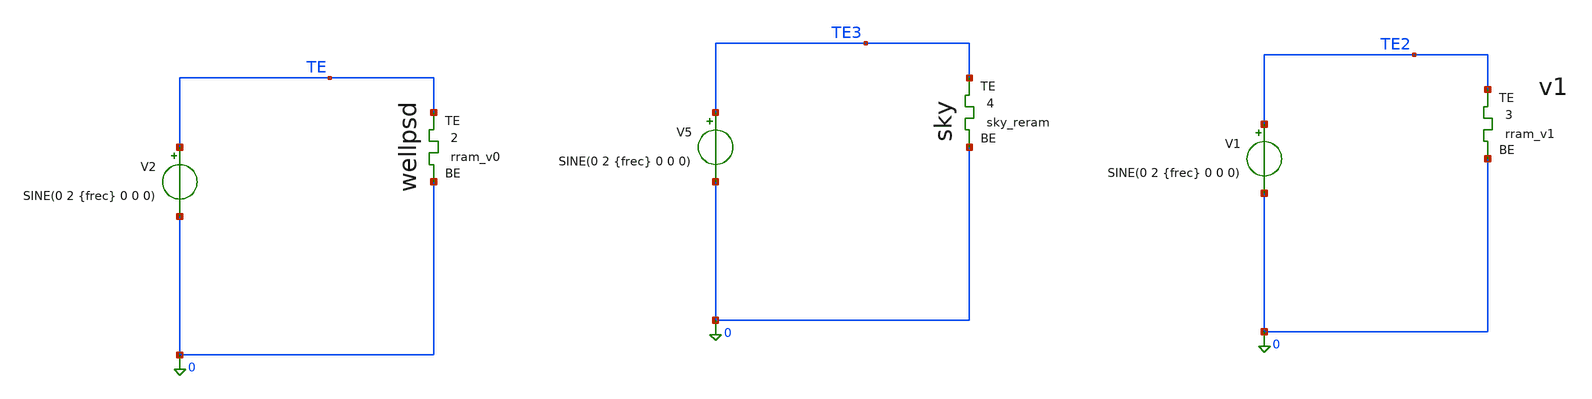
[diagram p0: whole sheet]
** sch_path: Memristor/tb_liss_rram_v0.sch
**.subckt tb_liss_rram_v0
V2 TE 0 SINE(0 2 {frec} 0 0 0)
X2 TE 0 rram_v0
X4 TE3 0 sky_reram
X3 TE2 0 rram_v1
V5 TE3 0 SINE(0 2 {frec} 0 0 0)
V1 TE2 0 SINE(0 2 {frec} 0 0 0)
**** begin user architecture code


.param frec=1k
.options num_threads=8
.tran 20n 1.2m uic
.save all
*.save ngap TE
.control

	run
	write tb_liss_rram_v0.raw
.endc




*MADE BY JORGE ALEJANDRO JUAREZ LORA IPN

.subckt rram_v0 TE BE
N1 TE BE rram_v0_model
.ends rram_v0

.subckt rram_v1 TE BE
N1 TE BE rram_v1_model gap_initial=0.2751
.ends rram_v0


.subckt sky_reram TE BE
N1 TE BE sky_reram_model Tfilament_0=3.3e-9
.ends sky_reram

.model rram_v0_model rram_v0_va
.model rram_v1_model rram_v1_va
.model sky_reram_model sky130_fd_pr_reram__reram_cell

.control
pre_osdi /foss/designs/SNN-MWIP/Memristor/rram_v0.osdi
pre_osdi /foss/designs/SNN-MWIP/Memristor/rram_v1.osdi
pre_osdi /foss/designs/SNN-MWIP/Memristor/sky.osdi
.endc

**** end user architecture code
**.ends
.end
